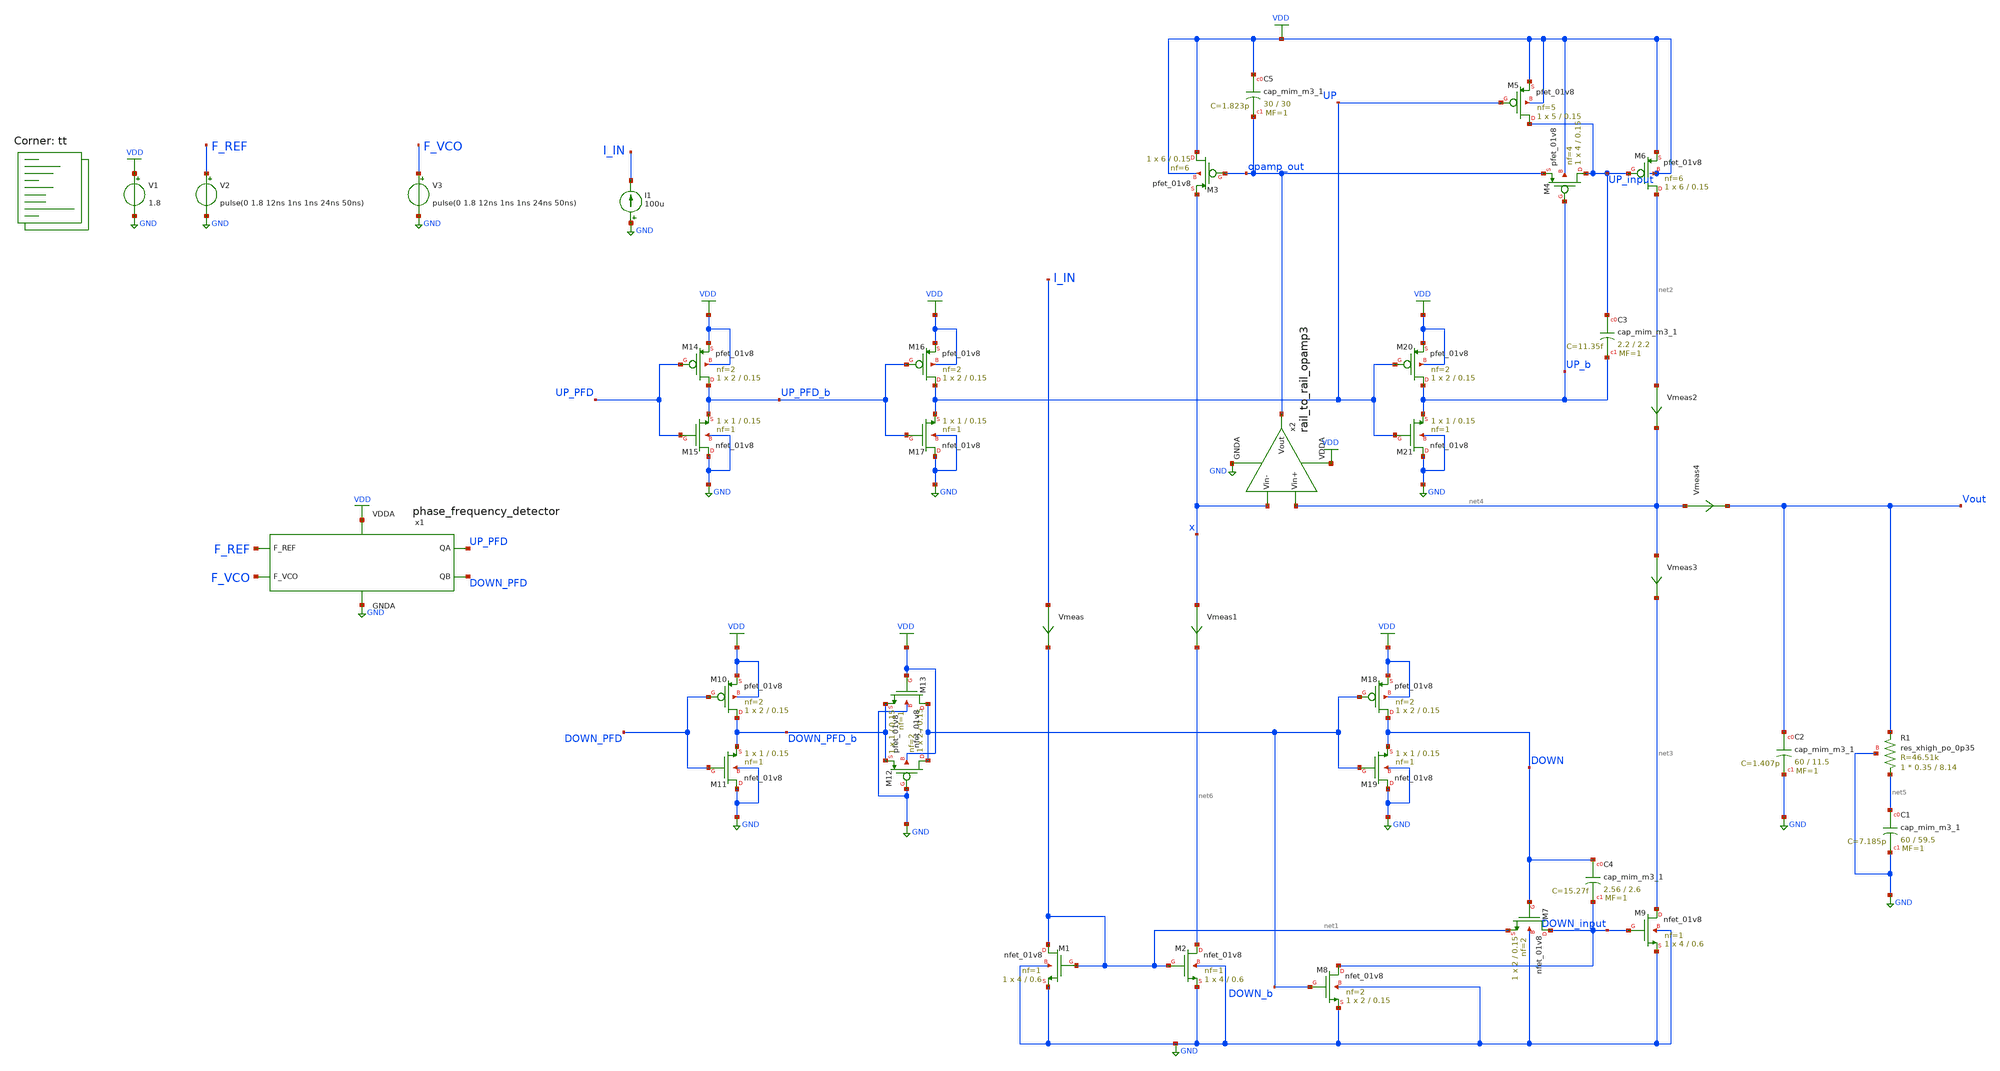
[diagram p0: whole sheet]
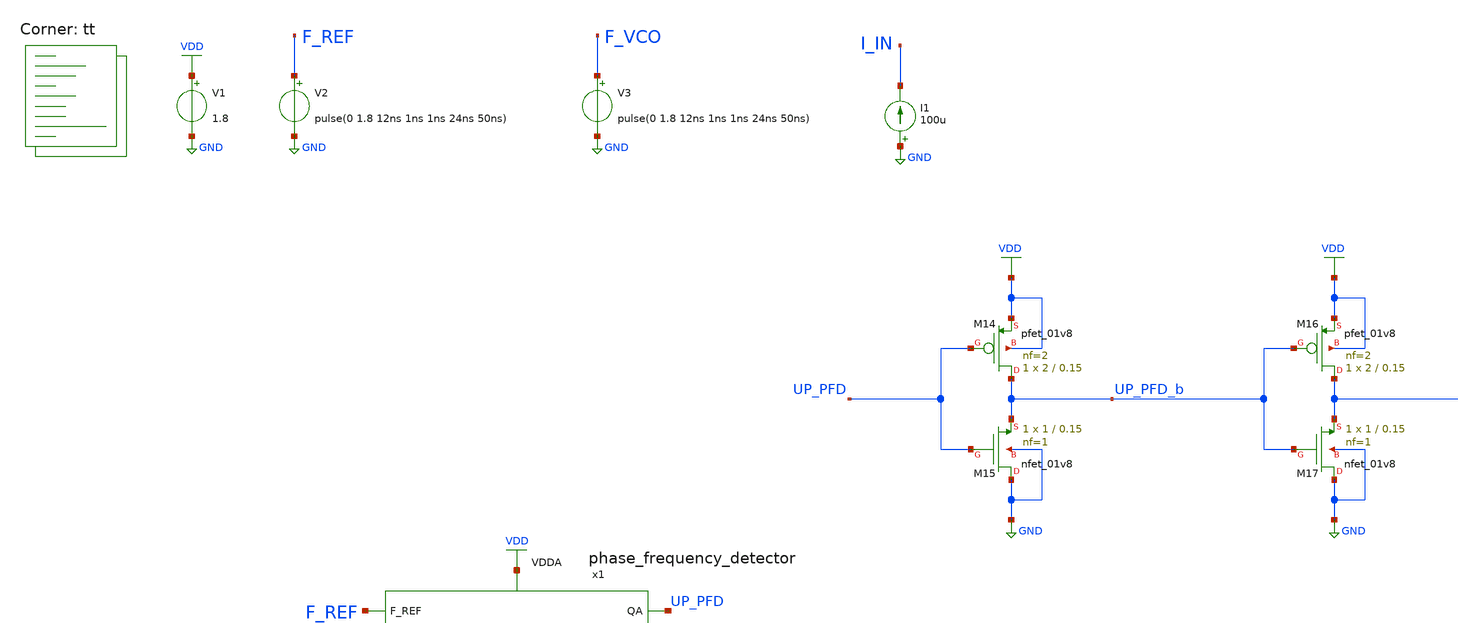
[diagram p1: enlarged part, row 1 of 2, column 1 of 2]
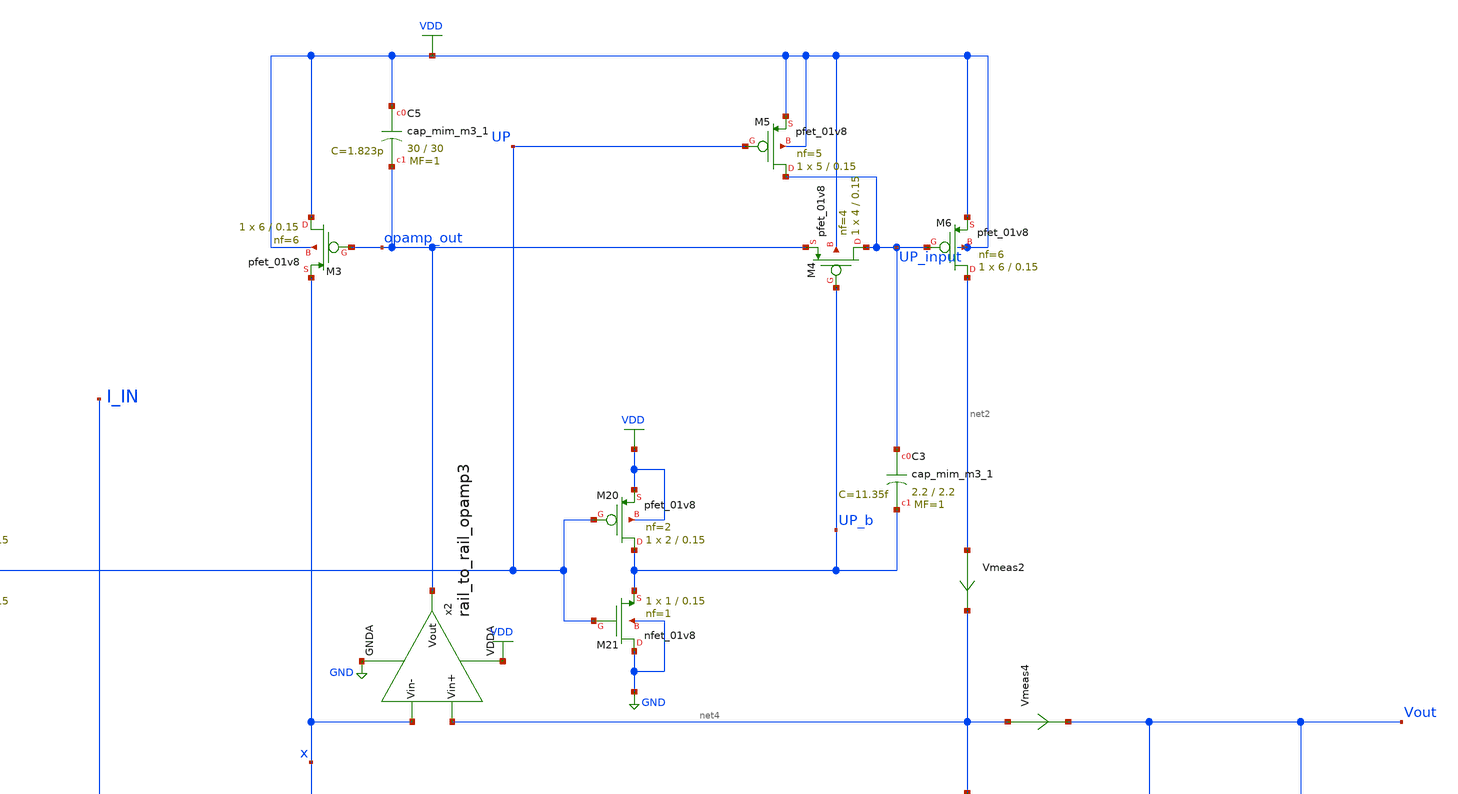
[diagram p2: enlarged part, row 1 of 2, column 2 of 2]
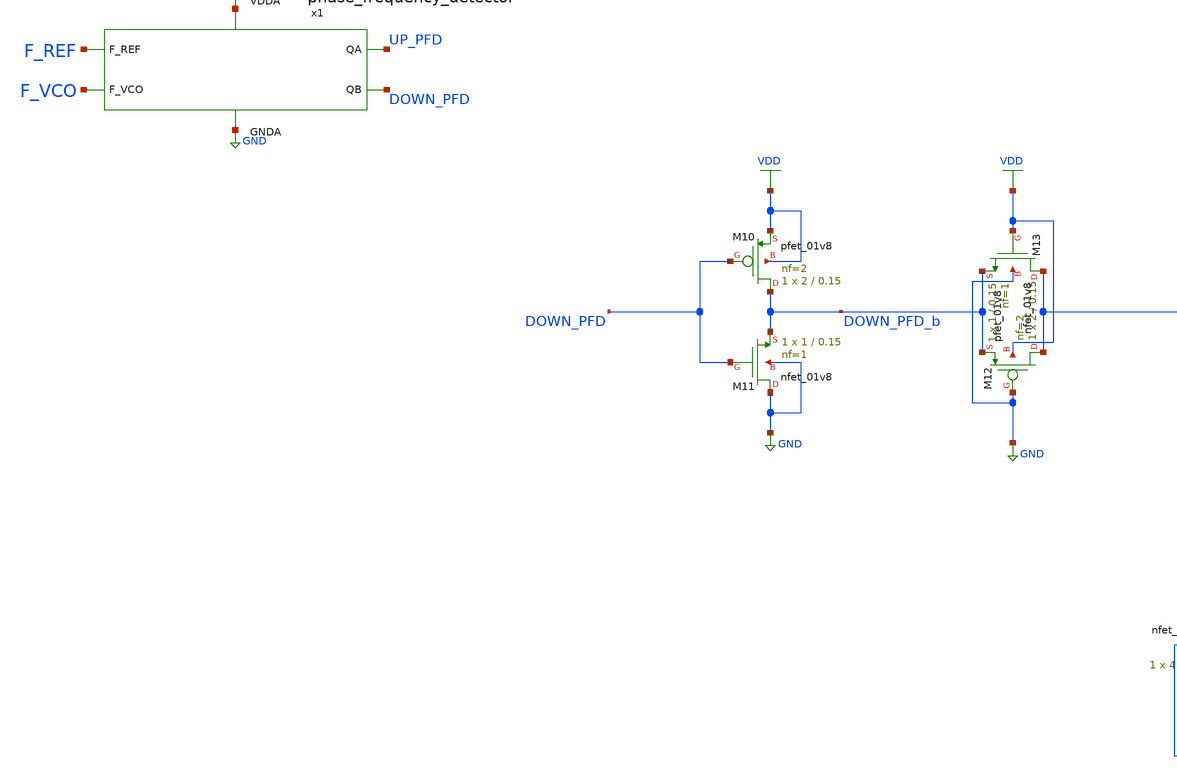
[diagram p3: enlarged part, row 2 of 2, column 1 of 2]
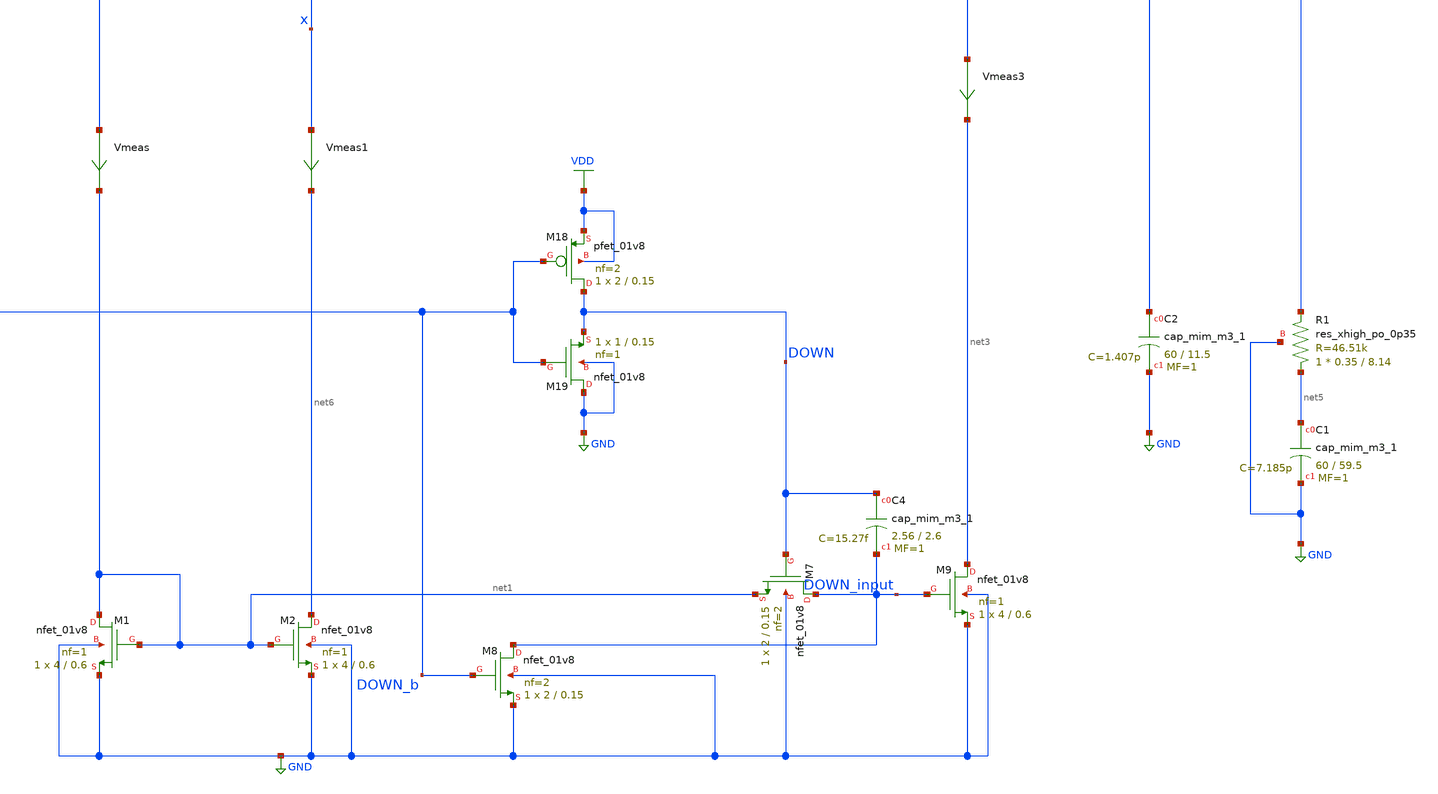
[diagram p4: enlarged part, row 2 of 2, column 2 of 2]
** sch_path: projects/pll/charge_pump/xschem_ngspice/pfd_charge_pump_dead_zone_check_4.sch
**.subckt pfd_charge_pump_dead_zone_check_4
V1 VDD GND 1.8
V2 F_REF GND pulse(0 1.8 12ns 1ns 1ns 24ns 50ns)
V3 F_VCO GND pulse(0 1.8 12ns 1ns 1ns 24ns 50ns)
x1 F_REF F_VCO VDD UP_PFD DOWN_PFD GND phase_frequency_detector
I1 GND I_IN 100u
XM1 net1 net1 GND GND sky130_fd_pr__nfet_01v8 L=0.6 W=4 nf=1 ad='int((nf+1)/2) * W/nf * 0.29' as='int((nf+2)/2) * W/nf * 0.29'
+ pd='2*int((nf+1)/2) * (W/nf + 0.29)' ps='2*int((nf+2)/2) * (W/nf + 0.29)' nrd='0.29 / W' nrs='0.29 / W'
+ sa=0 sb=0 sd=0 mult=1 m=1
XM2 net6 net1 GND GND sky130_fd_pr__nfet_01v8 L=0.6 W=4 nf=1 ad='int((nf+1)/2) * W/nf * 0.29' as='int((nf+2)/2) * W/nf * 0.29'
+ pd='2*int((nf+1)/2) * (W/nf + 0.29)' ps='2*int((nf+2)/2) * (W/nf + 0.29)' nrd='0.29 / W' nrs='0.29 / W'
+ sa=0 sb=0 sd=0 mult=1 m=1
XM3 VDD opamp_out x VDD sky130_fd_pr__pfet_01v8 L=0.15 W=6 nf=6 ad='int((nf+1)/2) * W/nf * 0.29' as='int((nf+2)/2) * W/nf * 0.29'
+ pd='2*int((nf+1)/2) * (W/nf + 0.29)' ps='2*int((nf+2)/2) * (W/nf + 0.29)' nrd='0.29 / W' nrs='0.29 / W'
+ sa=0 sb=0 sd=0 mult=1 m=1
XM4 UP_input UP_b opamp_out VDD sky130_fd_pr__pfet_01v8 L=0.15 W=4 nf=4 ad='int((nf+1)/2) * W/nf * 0.29'
+ as='int((nf+2)/2) * W/nf * 0.29' pd='2*int((nf+1)/2) * (W/nf + 0.29)' ps='2*int((nf+2)/2) * (W/nf + 0.29)'
+ nrd='0.29 / W' nrs='0.29 / W' sa=0 sb=0 sd=0 mult=1 m=1
XM5 UP_input UP VDD VDD sky130_fd_pr__pfet_01v8 L=0.15 W=5 nf=5 ad='int((nf+1)/2) * W/nf * 0.29' as='int((nf+2)/2) * W/nf * 0.29'
+ pd='2*int((nf+1)/2) * (W/nf + 0.29)' ps='2*int((nf+2)/2) * (W/nf + 0.29)' nrd='0.29 / W' nrs='0.29 / W'
+ sa=0 sb=0 sd=0 mult=1 m=1
XM6 net2 UP_input VDD VDD sky130_fd_pr__pfet_01v8 L=0.15 W=6 nf=6 ad='int((nf+1)/2) * W/nf * 0.29' as='int((nf+2)/2) * W/nf * 0.29'
+ pd='2*int((nf+1)/2) * (W/nf + 0.29)' ps='2*int((nf+2)/2) * (W/nf + 0.29)' nrd='0.29 / W' nrs='0.29 / W'
+ sa=0 sb=0 sd=0 mult=1 m=1
XM7 DOWN_input DOWN net1 GND sky130_fd_pr__nfet_01v8 L=0.15 W=2 nf=2 ad='int((nf+1)/2) * W/nf * 0.29'
+ as='int((nf+2)/2) * W/nf * 0.29' pd='2*int((nf+1)/2) * (W/nf + 0.29)' ps='2*int((nf+2)/2) * (W/nf + 0.29)'
+ nrd='0.29 / W' nrs='0.29 / W' sa=0 sb=0 sd=0 mult=1 m=1
XM8 DOWN_input DOWN_b GND GND sky130_fd_pr__nfet_01v8 L=0.15 W=2 nf=2 ad='int((nf+1)/2) * W/nf * 0.29'
+ as='int((nf+2)/2) * W/nf * 0.29' pd='2*int((nf+1)/2) * (W/nf + 0.29)' ps='2*int((nf+2)/2) * (W/nf + 0.29)'
+ nrd='0.29 / W' nrs='0.29 / W' sa=0 sb=0 sd=0 mult=1 m=1
XM9 net3 DOWN_input GND GND sky130_fd_pr__nfet_01v8 L=0.6 W=4 nf=1 ad='int((nf+1)/2) * W/nf * 0.29' as='int((nf+2)/2) * W/nf * 0.29'
+ pd='2*int((nf+1)/2) * (W/nf + 0.29)' ps='2*int((nf+2)/2) * (W/nf + 0.29)' nrd='0.29 / W' nrs='0.29 / W'
+ sa=0 sb=0 sd=0 mult=1 m=1
XC2 Vout GND sky130_fd_pr__cap_mim_m3_1 W=60 L=11.5 MF=1 m=1
XC1 net5 GND sky130_fd_pr__cap_mim_m3_1 W=60 L=59.5 MF=1 m=1
x2 VDD net4 x opamp_out GND rail_to_rail_opamp3
XR1 net5 Vout GND sky130_fd_pr__res_xhigh_po_0p35 L=8.14 mult=1 m=1
XM12 DOWN_b GND DOWN_PFD_b VDD sky130_fd_pr__pfet_01v8 L=0.15 W=2 nf=2 ad='int((nf+1)/2) * W/nf * 0.29'
+ as='int((nf+2)/2) * W/nf * 0.29' pd='2*int((nf+1)/2) * (W/nf + 0.29)' ps='2*int((nf+2)/2) * (W/nf + 0.29)'
+ nrd='0.29 / W' nrs='0.29 / W' sa=0 sb=0 sd=0 mult=1 m=1
XM13 DOWN_b VDD DOWN_PFD_b GND sky130_fd_pr__nfet_01v8 L=0.15 W=1 nf=1 ad='int((nf+1)/2) * W/nf * 0.29'
+ as='int((nf+2)/2) * W/nf * 0.29' pd='2*int((nf+1)/2) * (W/nf + 0.29)' ps='2*int((nf+2)/2) * (W/nf + 0.29)'
+ nrd='0.29 / W' nrs='0.29 / W' sa=0 sb=0 sd=0 mult=1 m=1
XC5 VDD opamp_out sky130_fd_pr__cap_mim_m3_1 W=30 L=30 MF=1 m=1
XM10 DOWN_PFD_b DOWN_PFD VDD VDD sky130_fd_pr__pfet_01v8 L=0.15 W=2 nf=2 ad='int((nf+1)/2) * W/nf * 0.29'
+ as='int((nf+2)/2) * W/nf * 0.29' pd='2*int((nf+1)/2) * (W/nf + 0.29)' ps='2*int((nf+2)/2) * (W/nf + 0.29)'
+ nrd='0.29 / W' nrs='0.29 / W' sa=0 sb=0 sd=0 mult=1 m=1
XM11 GND DOWN_PFD DOWN_PFD_b GND sky130_fd_pr__nfet_01v8 L=0.15 W=1 nf=1 ad='int((nf+1)/2) * W/nf * 0.29'
+ as='int((nf+2)/2) * W/nf * 0.29' pd='2*int((nf+1)/2) * (W/nf + 0.29)' ps='2*int((nf+2)/2) * (W/nf + 0.29)'
+ nrd='0.29 / W' nrs='0.29 / W' sa=0 sb=0 sd=0 mult=1 m=1
XM14 UP_PFD_b UP_PFD VDD VDD sky130_fd_pr__pfet_01v8 L=0.15 W=2 nf=2 ad='int((nf+1)/2) * W/nf * 0.29'
+ as='int((nf+2)/2) * W/nf * 0.29' pd='2*int((nf+1)/2) * (W/nf + 0.29)' ps='2*int((nf+2)/2) * (W/nf + 0.29)'
+ nrd='0.29 / W' nrs='0.29 / W' sa=0 sb=0 sd=0 mult=1 m=1
XM15 GND UP_PFD UP_PFD_b GND sky130_fd_pr__nfet_01v8 L=0.15 W=1 nf=1 ad='int((nf+1)/2) * W/nf * 0.29'
+ as='int((nf+2)/2) * W/nf * 0.29' pd='2*int((nf+1)/2) * (W/nf + 0.29)' ps='2*int((nf+2)/2) * (W/nf + 0.29)'
+ nrd='0.29 / W' nrs='0.29 / W' sa=0 sb=0 sd=0 mult=1 m=1
XM16 UP UP_PFD_b VDD VDD sky130_fd_pr__pfet_01v8 L=0.15 W=2 nf=2 ad='int((nf+1)/2) * W/nf * 0.29' as='int((nf+2)/2) * W/nf * 0.29'
+ pd='2*int((nf+1)/2) * (W/nf + 0.29)' ps='2*int((nf+2)/2) * (W/nf + 0.29)' nrd='0.29 / W' nrs='0.29 / W'
+ sa=0 sb=0 sd=0 mult=1 m=1
XM17 GND UP_PFD_b UP GND sky130_fd_pr__nfet_01v8 L=0.15 W=1 nf=1 ad='int((nf+1)/2) * W/nf * 0.29' as='int((nf+2)/2) * W/nf * 0.29'
+ pd='2*int((nf+1)/2) * (W/nf + 0.29)' ps='2*int((nf+2)/2) * (W/nf + 0.29)' nrd='0.29 / W' nrs='0.29 / W'
+ sa=0 sb=0 sd=0 mult=1 m=1
XM18 DOWN DOWN_b VDD VDD sky130_fd_pr__pfet_01v8 L=0.15 W=2 nf=2 ad='int((nf+1)/2) * W/nf * 0.29' as='int((nf+2)/2) * W/nf * 0.29'
+ pd='2*int((nf+1)/2) * (W/nf + 0.29)' ps='2*int((nf+2)/2) * (W/nf + 0.29)' nrd='0.29 / W' nrs='0.29 / W'
+ sa=0 sb=0 sd=0 mult=1 m=1
XM19 GND DOWN_b DOWN GND sky130_fd_pr__nfet_01v8 L=0.15 W=1 nf=1 ad='int((nf+1)/2) * W/nf * 0.29' as='int((nf+2)/2) * W/nf * 0.29'
+ pd='2*int((nf+1)/2) * (W/nf + 0.29)' ps='2*int((nf+2)/2) * (W/nf + 0.29)' nrd='0.29 / W' nrs='0.29 / W'
+ sa=0 sb=0 sd=0 mult=1 m=1
XM20 UP_b UP VDD VDD sky130_fd_pr__pfet_01v8 L=0.15 W=2 nf=2 ad='int((nf+1)/2) * W/nf * 0.29' as='int((nf+2)/2) * W/nf * 0.29'
+ pd='2*int((nf+1)/2) * (W/nf + 0.29)' ps='2*int((nf+2)/2) * (W/nf + 0.29)' nrd='0.29 / W' nrs='0.29 / W'
+ sa=0 sb=0 sd=0 mult=1 m=1
XM21 GND UP UP_b GND sky130_fd_pr__nfet_01v8 L=0.15 W=1 nf=1 ad='int((nf+1)/2) * W/nf * 0.29' as='int((nf+2)/2) * W/nf * 0.29'
+ pd='2*int((nf+1)/2) * (W/nf + 0.29)' ps='2*int((nf+2)/2) * (W/nf + 0.29)' nrd='0.29 / W' nrs='0.29 / W'
+ sa=0 sb=0 sd=0 mult=1 m=1
Vmeas I_IN net1 0
.save i(vmeas)
XC3 UP_input UP_b sky130_fd_pr__cap_mim_m3_1 W=2.2 L=2.2 MF=1 m=1
XC4 DOWN DOWN_input sky130_fd_pr__cap_mim_m3_1 W=2.56 L=2.6 MF=1 m=1
Vmeas1 x net6 0
.save i(vmeas1)
Vmeas2 net2 net4 0
.save i(vmeas2)
Vmeas3 net4 net3 0
.save i(vmeas3)
Vmeas4 net4 Vout 0
.save i(vmeas4)
**** begin user architecture code
.lib $::SKYWATER_MODELS/sky130.lib.spice tt



.include /foss/pdks/sky130A/libs.ref/sky130_fd_sc_hd/spice/sky130_fd_sc_hd.spice

.option method=gear
.option wnflag=1

.ic v(vout) = 0.9

.control
  let start_delay = 0ns
  let stop_delay = 24ns
  let index = -12
  dowhile start_delay <= stop_delay

    alter @V3[pulse] = [ 0 1.8 $&start_delay 1ns 1ns 24ns 50ns ]
    save i(vmeas2#branch) i(vmeas3#branch) i(vmeas4#branch) v(F_REF) v(F_VCO) v(vout)
    tran 5ps 1us
    remzerovec
    linearize i(vmeas2) i(vmeas3) i(vmeas4) v(F_REF) v(F_VCO) v(vout)
    echo $&start_delay
    write pfd_charge_pump_dead_zone_check_4_{$&index}.raw
    wrdata /foss/designs/my_design/projects/pll/charge_pump/xschem_ngspice/pfd_charge_pump_dead_zone_check_4_{$&index}.txt
+ i(vmeas4)
    set appendwrite
    reset
    let index = index + 1
    let start_delay = start_delay + 1ns

  end
.endc



**** end user architecture code
**.ends

* expanding   symbol:
*+  /foss/designs/my_design/projects/pll/pfd/xschem_ngspice/phase_frequency_detector.sym # of pins=6
** sym_path: projects/pll/pfd/xschem_ngspice/phase_frequency_detector.sym
** sch_path: projects/pll/pfd/xschem_ngspice/phase_frequency_detector.sch
.subckt phase_frequency_detector F_REF F_VCO VDDA QA QB GNDA
*.ipin F_REF
*.opin QA
*.ipin F_VCO
*.opin QB
*.ipin VDDA
*.ipin GNDA
x1 F_REF QA GNDA GNDA VDDA VDDA QA_b sky130_fd_sc_hd__nor2_1
x2 QA_b E GNDA GNDA VDDA VDDA QA sky130_fd_sc_hd__nor2_1
x3 QA_b E_b GNDA GNDA VDDA VDDA E sky130_fd_sc_hd__nor2_1
x4 E Reset GNDA GNDA VDDA VDDA E_b sky130_fd_sc_hd__nor2_1
x5 F_VCO QB GNDA GNDA VDDA VDDA QB_b sky130_fd_sc_hd__nor2_1
x6 QB_b F GNDA GNDA VDDA VDDA QB sky130_fd_sc_hd__nor2_1
x7 QB_b F_b GNDA GNDA VDDA VDDA F sky130_fd_sc_hd__nor2_1
x8 F Reset GNDA GNDA VDDA VDDA F_b sky130_fd_sc_hd__nor2_1
x9 QA QB GNDA GNDA VDDA VDDA before_Reset sky130_fd_sc_hd__nand2_1
x10 before_Reset GNDA GNDA VDDA VDDA net1 sky130_fd_sc_hd__inv_1
x11 net1 GNDA GNDA VDDA VDDA net2 sky130_fd_sc_hd__inv_1
x12 net2 GNDA GNDA VDDA VDDA net3 sky130_fd_sc_hd__inv_1
x13 net3 GNDA GNDA VDDA VDDA net4 sky130_fd_sc_hd__inv_1
x14 net4 GNDA GNDA VDDA VDDA Reset sky130_fd_sc_hd__inv_1
.ends


* expanding   symbol:
*+  /foss/designs/my_design/projects/pll/charge_pump/xschem_ngspice/rail_to_rail_opamp3.sym # of pins=5
** sym_path: projects/pll/charge_pump/xschem_ngspice/rail_to_rail_opamp3.sym
** sch_path: projects/pll/charge_pump/xschem_ngspice/rail_to_rail_opamp3.sch
.subckt rail_to_rail_opamp3 VDDA Vin+ Vin- Vout GNDA
*.opin Vout
*.ipin Vin+
*.ipin Vin-
*.ipin VDDA
*.ipin GNDA
XM2 n_left Vin+ v_common_n GNDA sky130_fd_pr__nfet_01v8 L=0.15 W=1 nf=1 ad='int((nf+1)/2) * W/nf * 0.29'
+ as='int((nf+2)/2) * W/nf * 0.29' pd='2*int((nf+1)/2) * (W/nf + 0.29)' ps='2*int((nf+2)/2) * (W/nf + 0.29)'
+ nrd='0.29 / W' nrs='0.29 / W' sa=0 sb=0 sd=0 mult=1 m=1
XM3 n_right Vin- v_common_n GNDA sky130_fd_pr__nfet_01v8 L=0.15 W=1 nf=1 ad='int((nf+1)/2) * W/nf * 0.29'
+ as='int((nf+2)/2) * W/nf * 0.29' pd='2*int((nf+1)/2) * (W/nf + 0.29)' ps='2*int((nf+2)/2) * (W/nf + 0.29)'
+ nrd='0.29 / W' nrs='0.29 / W' sa=0 sb=0 sd=0 mult=1 m=1
XM5 n_left n_left VDDA VDDA sky130_fd_pr__pfet_01v8 L=0.15 W=2 nf=2 ad='int((nf+1)/2) * W/nf * 0.29'
+ as='int((nf+2)/2) * W/nf * 0.29' pd='2*int((nf+1)/2) * (W/nf + 0.29)' ps='2*int((nf+2)/2) * (W/nf + 0.29)'
+ nrd='0.29 / W' nrs='0.29 / W' sa=0 sb=0 sd=0 mult=1 m=1
XM4 n_right n_left VDDA VDDA sky130_fd_pr__pfet_01v8 L=0.15 W=2 nf=2 ad='int((nf+1)/2) * W/nf * 0.29'
+ as='int((nf+2)/2) * W/nf * 0.29' pd='2*int((nf+1)/2) * (W/nf + 0.29)' ps='2*int((nf+2)/2) * (W/nf + 0.29)'
+ nrd='0.29 / W' nrs='0.29 / W' sa=0 sb=0 sd=0 mult=1 m=1
XM6 v_common_p p_bias VDDA VDDA sky130_fd_pr__pfet_01v8 L=0.15 W=3 nf=3 ad='int((nf+1)/2) * W/nf * 0.29'
+ as='int((nf+2)/2) * W/nf * 0.29' pd='2*int((nf+1)/2) * (W/nf + 0.29)' ps='2*int((nf+2)/2) * (W/nf + 0.29)'
+ nrd='0.29 / W' nrs='0.29 / W' sa=0 sb=0 sd=0 mult=1 m=1
XM7 p_left Vin+ v_common_p VDDA sky130_fd_pr__pfet_01v8 L=0.15 W=2 nf=2 ad='int((nf+1)/2) * W/nf * 0.29'
+ as='int((nf+2)/2) * W/nf * 0.29' pd='2*int((nf+1)/2) * (W/nf + 0.29)' ps='2*int((nf+2)/2) * (W/nf + 0.29)'
+ nrd='0.29 / W' nrs='0.29 / W' sa=0 sb=0 sd=0 mult=1 m=1
XM8 p_right Vin- v_common_p VDDA sky130_fd_pr__pfet_01v8 L=0.15 W=2 nf=2 ad='int((nf+1)/2) * W/nf * 0.29'
+ as='int((nf+2)/2) * W/nf * 0.29' pd='2*int((nf+1)/2) * (W/nf + 0.29)' ps='2*int((nf+2)/2) * (W/nf + 0.29)'
+ nrd='0.29 / W' nrs='0.29 / W' sa=0 sb=0 sd=0 mult=1 m=1
XM9 p_left p_left GNDA GNDA sky130_fd_pr__nfet_01v8 L=0.15 W=1 nf=1 ad='int((nf+1)/2) * W/nf * 0.29'
+ as='int((nf+2)/2) * W/nf * 0.29' pd='2*int((nf+1)/2) * (W/nf + 0.29)' ps='2*int((nf+2)/2) * (W/nf + 0.29)'
+ nrd='0.29 / W' nrs='0.29 / W' sa=0 sb=0 sd=0 mult=1 m=1
XM10 p_right p_left GNDA GNDA sky130_fd_pr__nfet_01v8 L=0.15 W=1 nf=1 ad='int((nf+1)/2) * W/nf * 0.29'
+ as='int((nf+2)/2) * W/nf * 0.29' pd='2*int((nf+1)/2) * (W/nf + 0.29)' ps='2*int((nf+2)/2) * (W/nf + 0.29)'
+ nrd='0.29 / W' nrs='0.29 / W' sa=0 sb=0 sd=0 mult=1 m=1
XM1 v_common_n n_bias GNDA GNDA sky130_fd_pr__nfet_01v8 L=0.15 W=1 nf=1 ad='int((nf+1)/2) * W/nf * 0.29'
+ as='int((nf+2)/2) * W/nf * 0.29' pd='2*int((nf+1)/2) * (W/nf + 0.29)' ps='2*int((nf+2)/2) * (W/nf + 0.29)'
+ nrd='0.29 / W' nrs='0.29 / W' sa=0 sb=0 sd=0 mult=1 m=1
XM11 Vout n_right VDDA VDDA sky130_fd_pr__pfet_01v8 L=0.15 W=16 nf=2 ad='int((nf+1)/2) * W/nf * 0.29'
+ as='int((nf+2)/2) * W/nf * 0.29' pd='2*int((nf+1)/2) * (W/nf + 0.29)' ps='2*int((nf+2)/2) * (W/nf + 0.29)'
+ nrd='0.29 / W' nrs='0.29 / W' sa=0 sb=0 sd=0 mult=1 m=1
XM12 Vout p_right GNDA GNDA sky130_fd_pr__nfet_01v8 L=0.15 W=8 nf=1 ad='int((nf+1)/2) * W/nf * 0.29'
+ as='int((nf+2)/2) * W/nf * 0.29' pd='2*int((nf+1)/2) * (W/nf + 0.29)' ps='2*int((nf+2)/2) * (W/nf + 0.29)'
+ nrd='0.29 / W' nrs='0.29 / W' sa=0 sb=0 sd=0 mult=1 m=1
XM13 n_bias n_bias GNDA GNDA sky130_fd_pr__nfet_01v8 L=0.15 W=1 nf=1 ad='int((nf+1)/2) * W/nf * 0.29'
+ as='int((nf+2)/2) * W/nf * 0.29' pd='2*int((nf+1)/2) * (W/nf + 0.29)' ps='2*int((nf+2)/2) * (W/nf + 0.29)'
+ nrd='0.29 / W' nrs='0.29 / W' sa=0 sb=0 sd=0 mult=1 m=1
XM15 p_bias p_bias VDDA VDDA sky130_fd_pr__pfet_01v8 L=0.15 W=2 nf=2 ad='int((nf+1)/2) * W/nf * 0.29'
+ as='int((nf+2)/2) * W/nf * 0.29' pd='2*int((nf+1)/2) * (W/nf + 0.29)' ps='2*int((nf+2)/2) * (W/nf + 0.29)'
+ nrd='0.29 / W' nrs='0.29 / W' sa=0 sb=0 sd=0 mult=1 m=1
Vmeas net1 n_bias 0
.save i(vmeas)
XM14 net1 net1 p_bias p_bias sky130_fd_pr__pfet_01v8 L=0.15 W=2 nf=2 ad='int((nf+1)/2) * W/nf * 0.29'
+ as='int((nf+2)/2) * W/nf * 0.29' pd='2*int((nf+1)/2) * (W/nf + 0.29)' ps='2*int((nf+2)/2) * (W/nf + 0.29)'
+ nrd='0.29 / W' nrs='0.29 / W' sa=0 sb=0 sd=0 mult=1 m=1
.ends

.GLOBAL GND
.GLOBAL VDD
.end
